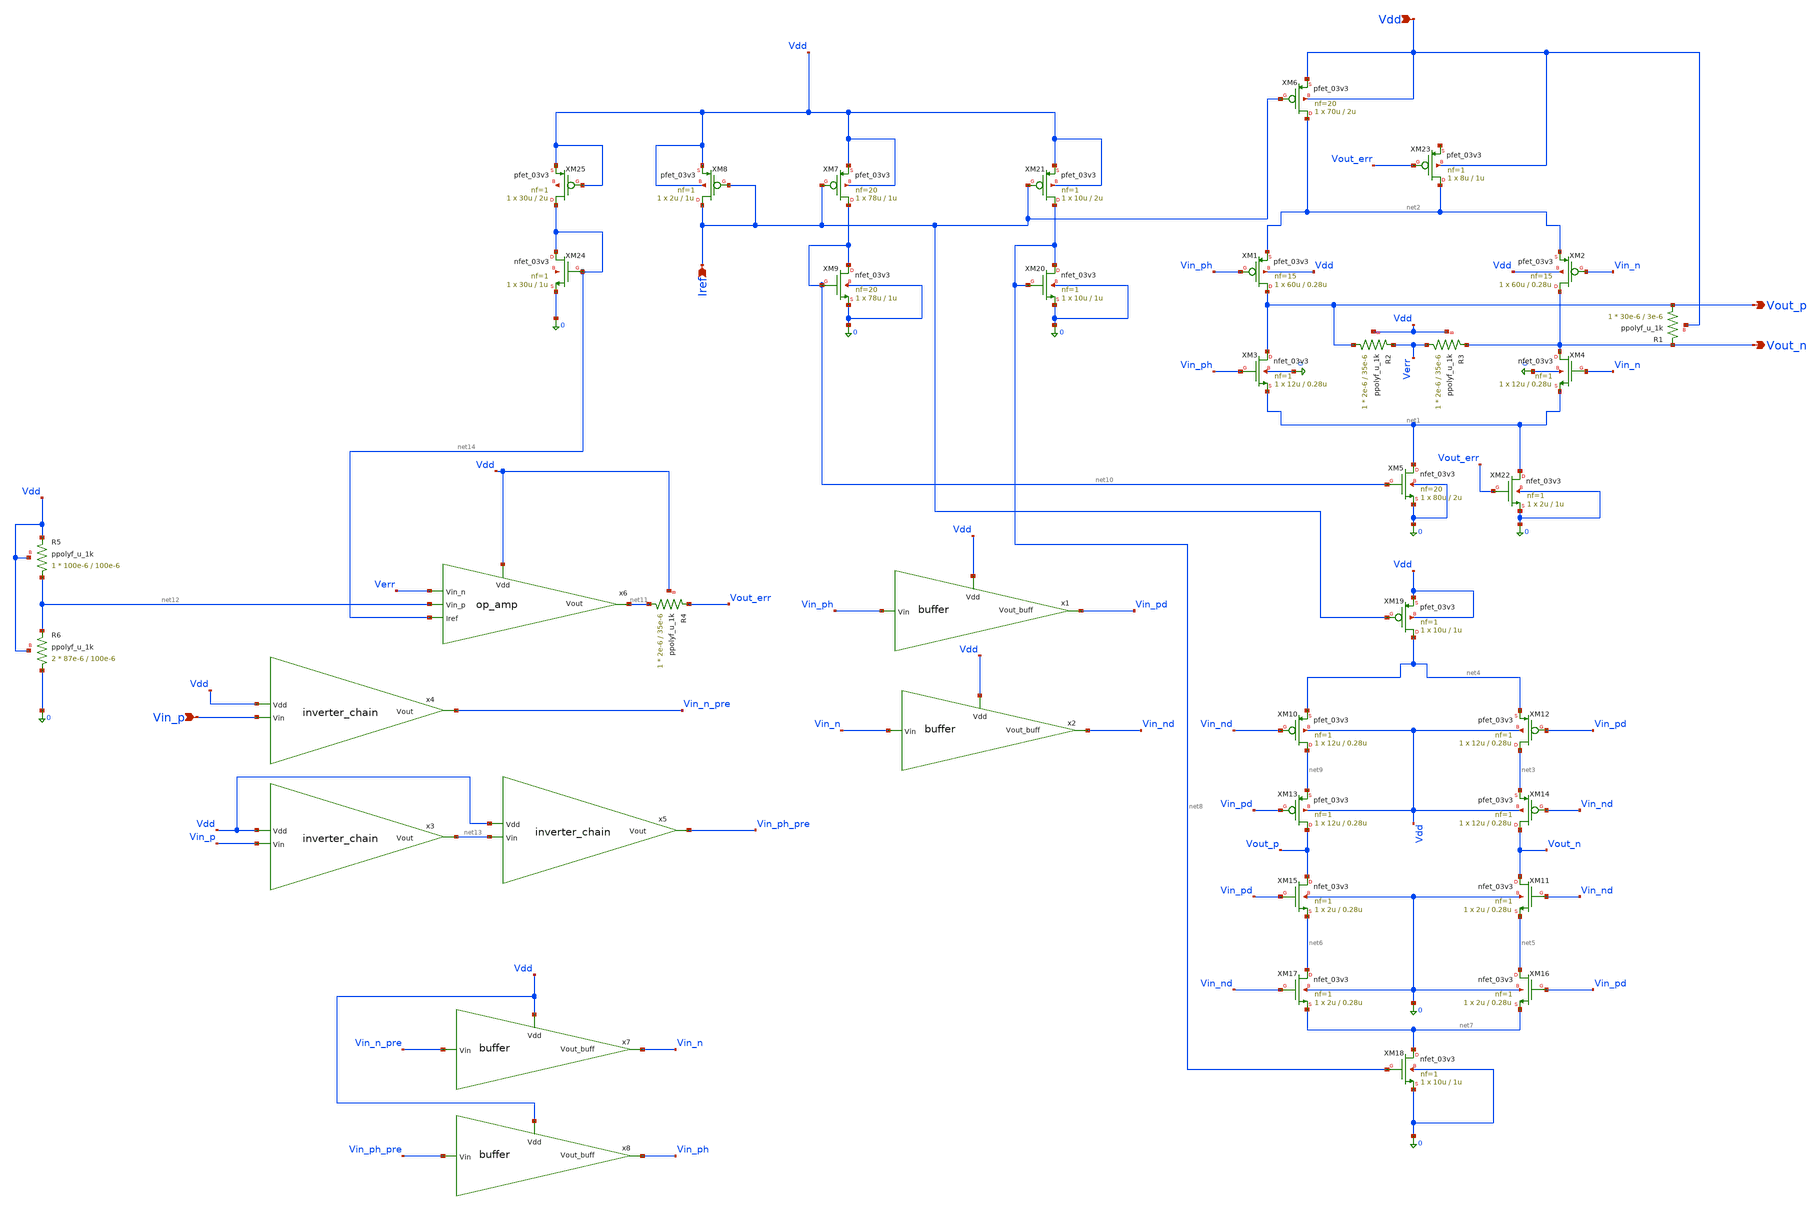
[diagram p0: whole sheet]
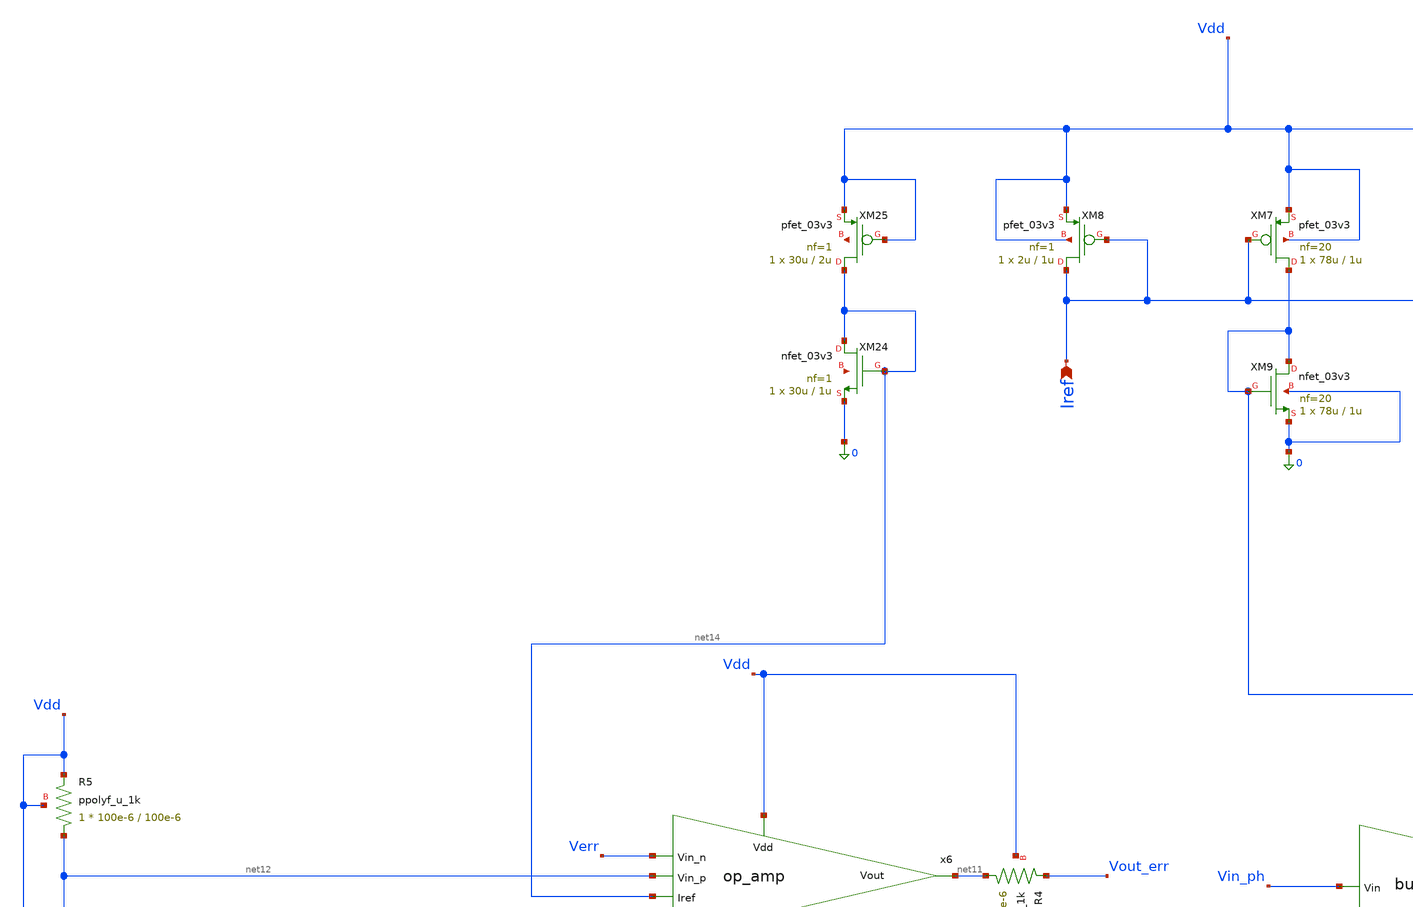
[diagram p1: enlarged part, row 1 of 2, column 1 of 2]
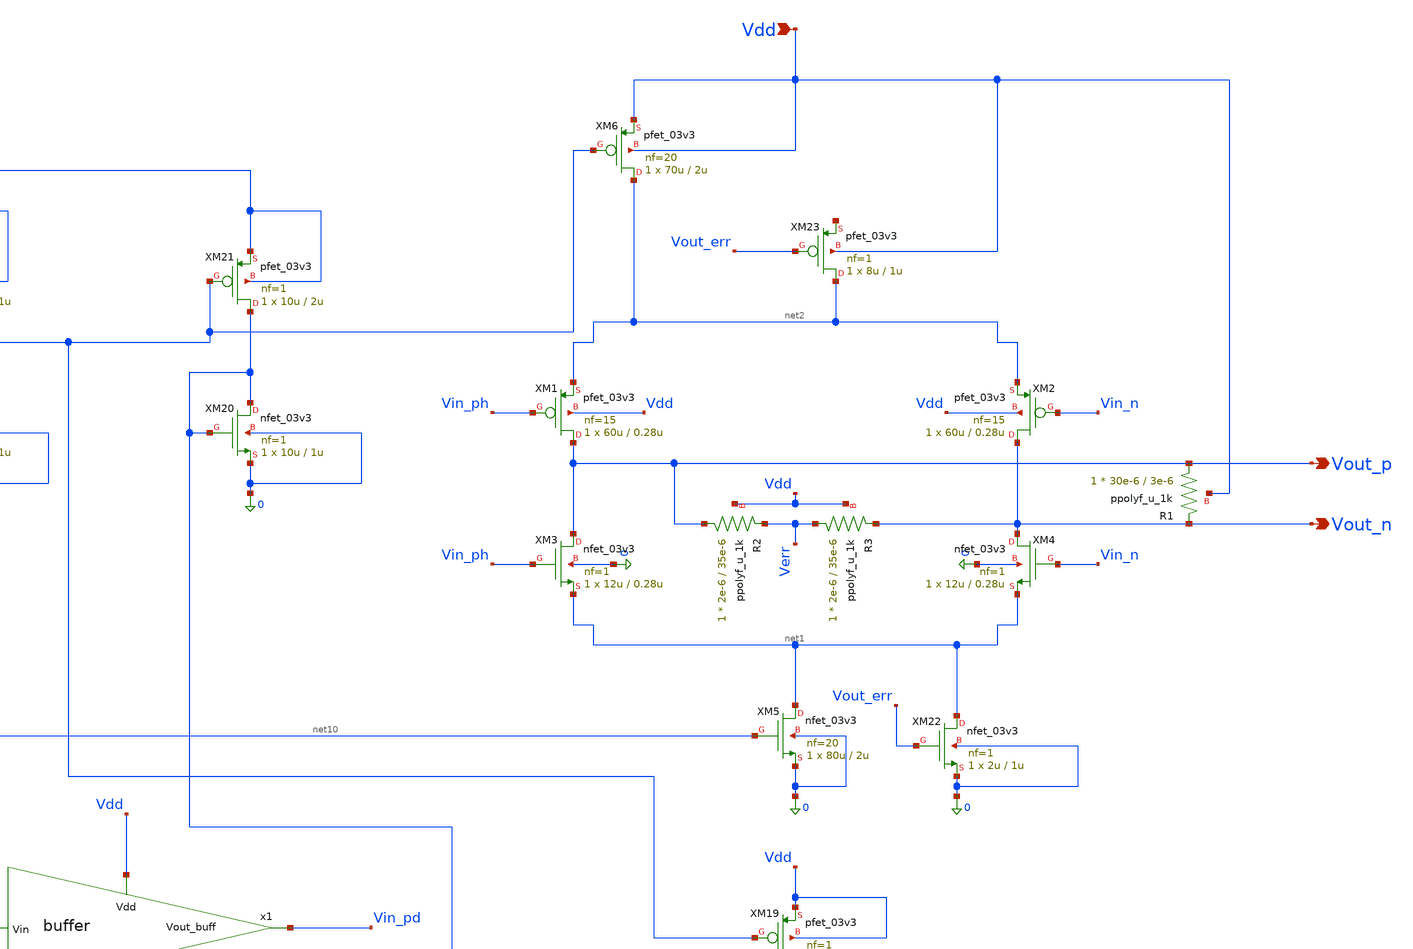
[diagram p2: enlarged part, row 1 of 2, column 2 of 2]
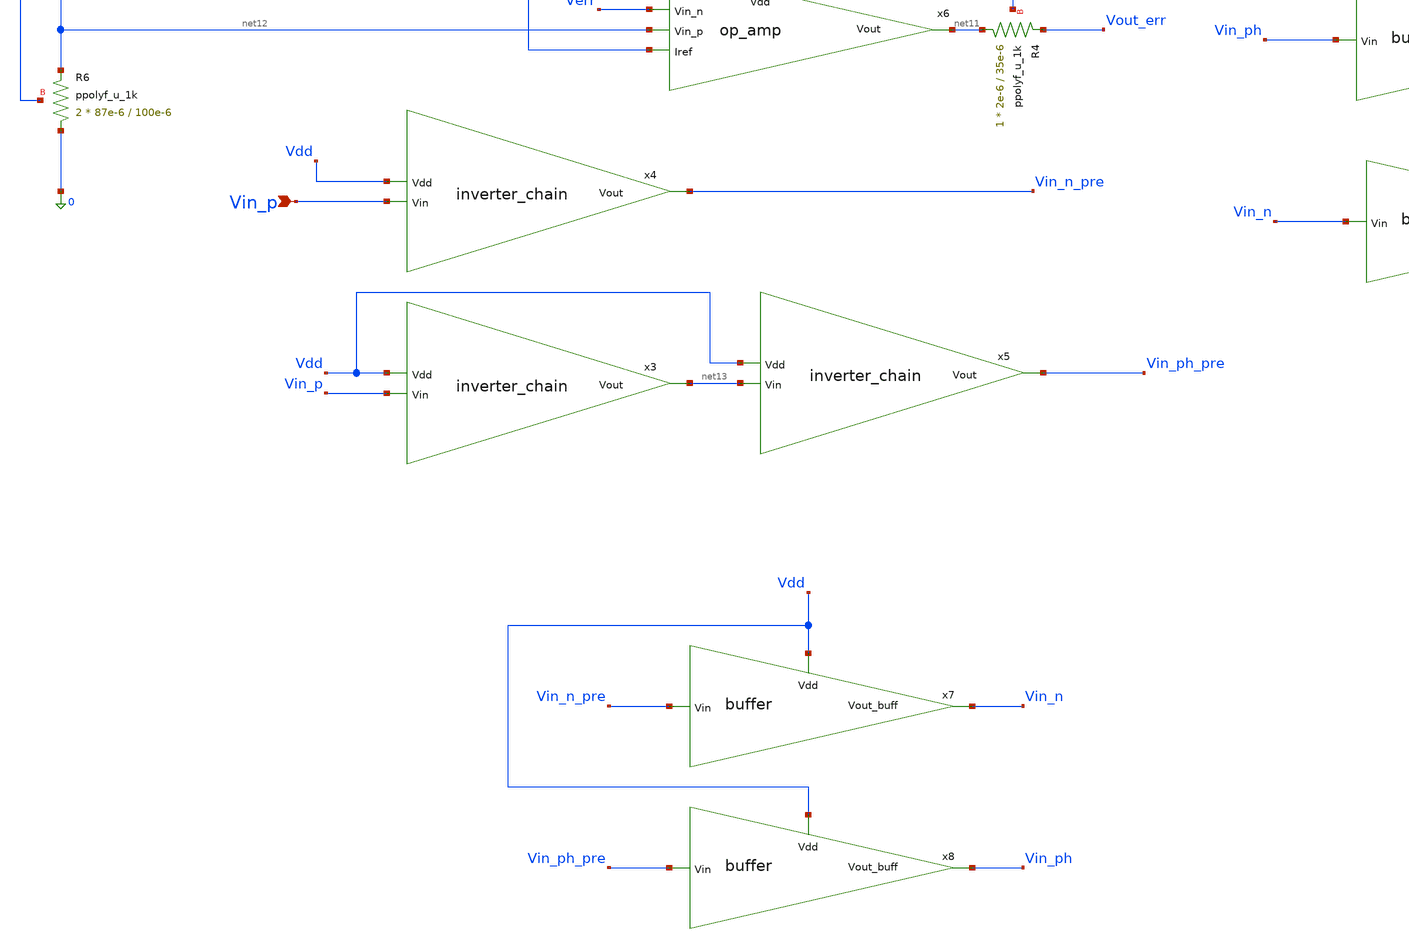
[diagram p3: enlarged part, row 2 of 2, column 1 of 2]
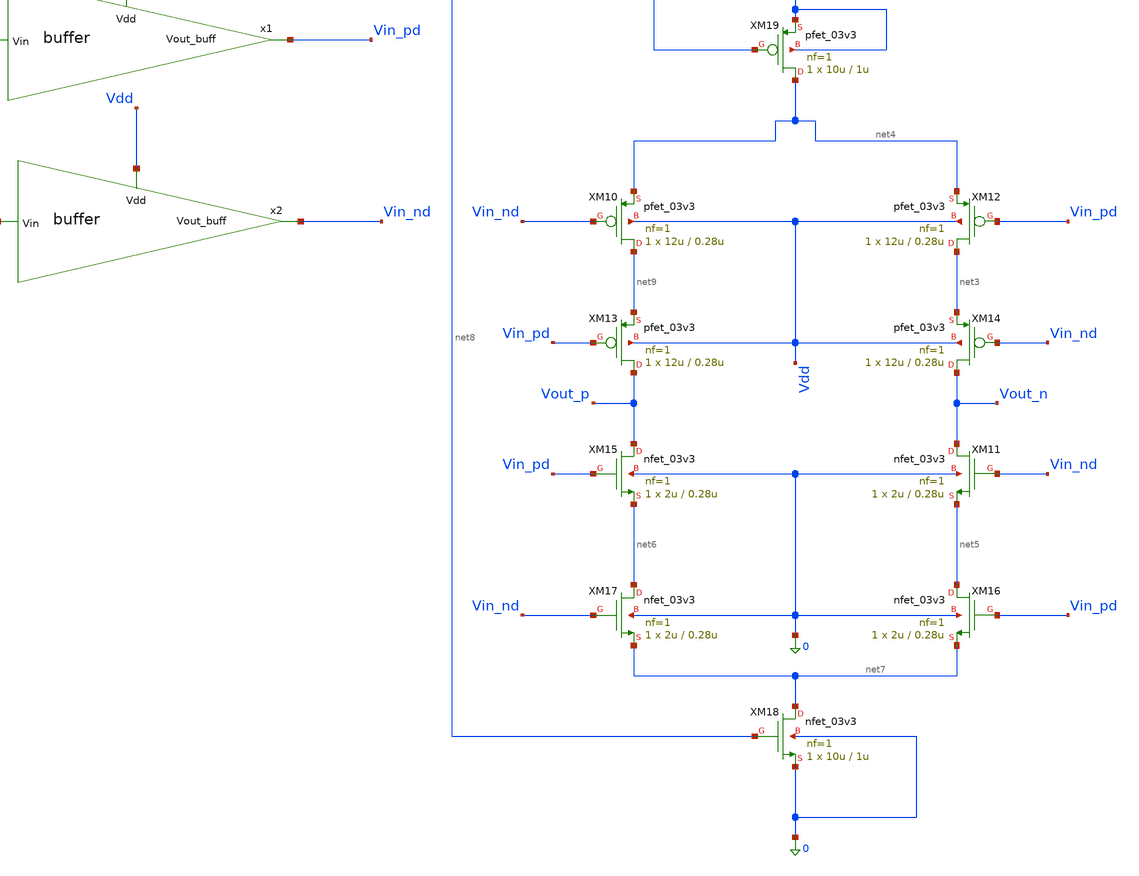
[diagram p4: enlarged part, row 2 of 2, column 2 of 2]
** sch_path: blocks/adc/lvds/lvds_v5.sch
**.subckt lvds_v5 Vdd Iref Vin_p Vout_n Vout_p
*.ipin Vdd
*.ipin Iref
*.ipin Vin_p
*.opin Vout_n
*.opin Vout_p
XM1 Vout_p Vin_ph net2 Vdd pfet_03v3 L=0.28u W=60u nf=15 ad='int((nf+1)/2) * W/nf * 0.18u' as='int((nf+2)/2) * W/nf * 0.18u'
+ pd='2*int((nf+1)/2) * (W/nf + 0.18u)' ps='2*int((nf+2)/2) * (W/nf + 0.18u)' nrd='0.18u / W' nrs='0.18u / W'
+ sa=0 sb=0 sd=0 m=1
XM2 Vout_n Vin_n net2 Vdd pfet_03v3 L=0.28u W=60u nf=15 ad='int((nf+1)/2) * W/nf * 0.18u' as='int((nf+2)/2) * W/nf * 0.18u'
+ pd='2*int((nf+1)/2) * (W/nf + 0.18u)' ps='2*int((nf+2)/2) * (W/nf + 0.18u)' nrd='0.18u / W' nrs='0.18u / W'
+ sa=0 sb=0 sd=0 m=1
XM3 Vout_p Vin_ph net1 0 nfet_03v3 L=0.28u W=12u nf=1 ad='int((nf+1)/2) * W/nf * 0.18u' as='int((nf+2)/2) * W/nf * 0.18u'
+ pd='2*int((nf+1)/2) * (W/nf + 0.18u)' ps='2*int((nf+2)/2) * (W/nf + 0.18u)' nrd='0.18u / W' nrs='0.18u / W'
+ sa=0 sb=0 sd=0 m=1
XM4 Vout_n Vin_n net1 0 nfet_03v3 L=0.28u W=12u nf=1 ad='int((nf+1)/2) * W/nf * 0.18u' as='int((nf+2)/2) * W/nf * 0.18u'
+ pd='2*int((nf+1)/2) * (W/nf + 0.18u)' ps='2*int((nf+2)/2) * (W/nf + 0.18u)' nrd='0.18u / W' nrs='0.18u / W'
+ sa=0 sb=0 sd=0 m=1
XM5 net1 net10 0 0 nfet_03v3 L=2u W=80u nf=20 ad='int((nf+1)/2) * W/nf * 0.18u' as='int((nf+2)/2) * W/nf * 0.18u'
+ pd='2*int((nf+1)/2) * (W/nf + 0.18u)' ps='2*int((nf+2)/2) * (W/nf + 0.18u)' nrd='0.18u / W' nrs='0.18u / W'
+ sa=0 sb=0 sd=0 m=1
XM6 net2 Iref Vdd Vdd pfet_03v3 L=2u W=70u nf=20 ad='int((nf+1)/2) * W/nf * 0.18u' as='int((nf+2)/2) * W/nf * 0.18u'
+ pd='2*int((nf+1)/2) * (W/nf + 0.18u)' ps='2*int((nf+2)/2) * (W/nf + 0.18u)' nrd='0.18u / W' nrs='0.18u / W'
+ sa=0 sb=0 sd=0 m=1
XM8 Iref Iref Vdd Vdd pfet_03v3 L=1u W=2u nf=1 ad='int((nf+1)/2) * W/nf * 0.18u' as='int((nf+2)/2) * W/nf * 0.18u'
+ pd='2*int((nf+1)/2) * (W/nf + 0.18u)' ps='2*int((nf+2)/2) * (W/nf + 0.18u)' nrd='0.18u / W' nrs='0.18u / W'
+ sa=0 sb=0 sd=0 m=1
XM10 net9 Vin_nd net4 Vdd pfet_03v3 L=0.28u W=12u nf=1 ad='int((nf+1)/2) * W/nf * 0.18u' as='int((nf+2)/2) * W/nf * 0.18u'
+ pd='2*int((nf+1)/2) * (W/nf + 0.18u)' ps='2*int((nf+2)/2) * (W/nf + 0.18u)' nrd='0.18u / W' nrs='0.18u / W'
+ sa=0 sb=0 sd=0 m=1
XM11 Vout_n Vin_nd net5 0 nfet_03v3 L=0.28u W=2u nf=1 ad='int((nf+1)/2) * W/nf * 0.18u' as='int((nf+2)/2) * W/nf * 0.18u'
+ pd='2*int((nf+1)/2) * (W/nf + 0.18u)' ps='2*int((nf+2)/2) * (W/nf + 0.18u)' nrd='0.18u / W' nrs='0.18u / W'
+ sa=0 sb=0 sd=0 m=1
XM12 net3 Vin_pd net4 Vdd pfet_03v3 L=0.28u W=12u nf=1 ad='int((nf+1)/2) * W/nf * 0.18u' as='int((nf+2)/2) * W/nf * 0.18u'
+ pd='2*int((nf+1)/2) * (W/nf + 0.18u)' ps='2*int((nf+2)/2) * (W/nf + 0.18u)' nrd='0.18u / W' nrs='0.18u / W'
+ sa=0 sb=0 sd=0 m=1
XM13 Vout_p Vin_pd net9 Vdd pfet_03v3 L=0.28u W=12u nf=1 ad='int((nf+1)/2) * W/nf * 0.18u' as='int((nf+2)/2) * W/nf * 0.18u'
+ pd='2*int((nf+1)/2) * (W/nf + 0.18u)' ps='2*int((nf+2)/2) * (W/nf + 0.18u)' nrd='0.18u / W' nrs='0.18u / W'
+ sa=0 sb=0 sd=0 m=1
XM14 Vout_n Vin_nd net3 Vdd pfet_03v3 L=0.28u W=12u nf=1 ad='int((nf+1)/2) * W/nf * 0.18u' as='int((nf+2)/2) * W/nf * 0.18u'
+ pd='2*int((nf+1)/2) * (W/nf + 0.18u)' ps='2*int((nf+2)/2) * (W/nf + 0.18u)' nrd='0.18u / W' nrs='0.18u / W'
+ sa=0 sb=0 sd=0 m=1
XM15 Vout_p Vin_pd net6 0 nfet_03v3 L=0.28u W=2u nf=1 ad='int((nf+1)/2) * W/nf * 0.18u' as='int((nf+2)/2) * W/nf * 0.18u'
+ pd='2*int((nf+1)/2) * (W/nf + 0.18u)' ps='2*int((nf+2)/2) * (W/nf + 0.18u)' nrd='0.18u / W' nrs='0.18u / W'
+ sa=0 sb=0 sd=0 m=1
XM16 net5 Vin_pd net7 0 nfet_03v3 L=0.28u W=2u nf=1 ad='int((nf+1)/2) * W/nf * 0.18u' as='int((nf+2)/2) * W/nf * 0.18u'
+ pd='2*int((nf+1)/2) * (W/nf + 0.18u)' ps='2*int((nf+2)/2) * (W/nf + 0.18u)' nrd='0.18u / W' nrs='0.18u / W'
+ sa=0 sb=0 sd=0 m=1
XM17 net6 Vin_nd net7 0 nfet_03v3 L=0.28u W=2u nf=1 ad='int((nf+1)/2) * W/nf * 0.18u' as='int((nf+2)/2) * W/nf * 0.18u'
+ pd='2*int((nf+1)/2) * (W/nf + 0.18u)' ps='2*int((nf+2)/2) * (W/nf + 0.18u)' nrd='0.18u / W' nrs='0.18u / W'
+ sa=0 sb=0 sd=0 m=1
XM18 net7 net8 0 0 nfet_03v3 L=1u W=10u nf=1 ad='int((nf+1)/2) * W/nf * 0.18u' as='int((nf+2)/2) * W/nf * 0.18u'
+ pd='2*int((nf+1)/2) * (W/nf + 0.18u)' ps='2*int((nf+2)/2) * (W/nf + 0.18u)' nrd='0.18u / W' nrs='0.18u / W'
+ sa=0 sb=0 sd=0 m=1
XM19 net4 Iref Vdd Vdd pfet_03v3 L=1u W=10u nf=1 ad='int((nf+1)/2) * W/nf * 0.18u' as='int((nf+2)/2) * W/nf * 0.18u'
+ pd='2*int((nf+1)/2) * (W/nf + 0.18u)' ps='2*int((nf+2)/2) * (W/nf + 0.18u)' nrd='0.18u / W' nrs='0.18u / W'
+ sa=0 sb=0 sd=0 m=1
XM21 net8 Iref Vdd Vdd pfet_03v3 L=2u W=10u nf=1 ad='int((nf+1)/2) * W/nf * 0.18u' as='int((nf+2)/2) * W/nf * 0.18u'
+ pd='2*int((nf+1)/2) * (W/nf + 0.18u)' ps='2*int((nf+2)/2) * (W/nf + 0.18u)' nrd='0.18u / W' nrs='0.18u / W'
+ sa=0 sb=0 sd=0 m=1
XM20 net8 net8 0 0 nfet_03v3 L=1u W=10u nf=1 ad='int((nf+1)/2) * W/nf * 0.18u' as='int((nf+2)/2) * W/nf * 0.18u'
+ pd='2*int((nf+1)/2) * (W/nf + 0.18u)' ps='2*int((nf+2)/2) * (W/nf + 0.18u)' nrd='0.18u / W' nrs='0.18u / W'
+ sa=0 sb=0 sd=0 m=1
XR2 Vout_p Verr Vdd ppolyf_u_1k r_width=2e-6 r_length=35e-6 m=1
XR3 Verr Vout_n Vdd ppolyf_u_1k r_width=2e-6 r_length=35e-6 m=1
XM7 net10 Iref Vdd Vdd pfet_03v3 L=1u W=78u nf=20 ad='int((nf+1)/2) * W/nf * 0.18u' as='int((nf+2)/2) * W/nf * 0.18u'
+ pd='2*int((nf+1)/2) * (W/nf + 0.18u)' ps='2*int((nf+2)/2) * (W/nf + 0.18u)' nrd='0.18u / W' nrs='0.18u / W'
+ sa=0 sb=0 sd=0 m=1
XM9 net10 net10 0 0 nfet_03v3 L=1u W=78u nf=20 ad='int((nf+1)/2) * W/nf * 0.18u' as='int((nf+2)/2) * W/nf * 0.18u'
+ pd='2*int((nf+1)/2) * (W/nf + 0.18u)' ps='2*int((nf+2)/2) * (W/nf + 0.18u)' nrd='0.18u / W' nrs='0.18u / W'
+ sa=0 sb=0 sd=0 m=1
x4 Vdd Vin_n_pre Vin_p inverter_chain
XM22 net1 Vout_err 0 0 nfet_03v3 L=1u W=2u nf=1 ad='int((nf+1)/2) * W/nf * 0.18u' as='int((nf+2)/2) * W/nf * 0.18u'
+ pd='2*int((nf+1)/2) * (W/nf + 0.18u)' ps='2*int((nf+2)/2) * (W/nf + 0.18u)' nrd='0.18u / W' nrs='0.18u / W'
+ sa=0 sb=0 sd=0 m=1
XM23 net2 Vout_err net15 Vdd pfet_03v3 L=1u W=8u nf=1 ad='int((nf+1)/2) * W/nf * 0.18u' as='int((nf+2)/2) * W/nf * 0.18u'
+ pd='2*int((nf+1)/2) * (W/nf + 0.18u)' ps='2*int((nf+2)/2) * (W/nf + 0.18u)' nrd='0.18u / W' nrs='0.18u / W'
+ sa=0 sb=0 sd=0 m=1
x3 Vdd net13 Vin_p inverter_chain
x5 Vdd Vin_ph_pre net13 inverter_chain
x7 Vdd Vin_n Vin_n_pre buffer
x8 Vdd Vin_ph Vin_ph_pre buffer
XM24 net14 net14 0 net16 nfet_03v3 L=1u W=30u nf=1 ad='int((nf+1)/2) * W/nf * 0.18u' as='int((nf+2)/2) * W/nf * 0.18u'
+ pd='2*int((nf+1)/2) * (W/nf + 0.18u)' ps='2*int((nf+2)/2) * (W/nf + 0.18u)' nrd='0.18u / W' nrs='0.18u / W'
+ sa=0 sb=0 sd=0 m=1
XM25 net14 Vdd Vdd net17 pfet_03v3 L=2u W=30u nf=1 ad='int((nf+1)/2) * W/nf * 0.18u' as='int((nf+2)/2) * W/nf * 0.18u'
+ pd='2*int((nf+1)/2) * (W/nf + 0.18u)' ps='2*int((nf+2)/2) * (W/nf + 0.18u)' nrd='0.18u / W' nrs='0.18u / W'
+ sa=0 sb=0 sd=0 m=1
x1 Vdd Vin_pd Vin_ph buffer
x2 Vdd Vin_nd Vin_n buffer
XR4 net11 Vout_err Vdd ppolyf_u_1k r_width=2e-6 r_length=35e-6 m=1
x6 Vdd net11 Verr net12 net14 op_amp
XR1 Vout_p Vout_n Vdd ppolyf_u_1k r_width=30e-6 r_length=3e-6 m=1
XR5 net12 Vdd Vdd ppolyf_u_1k r_width=100e-6 r_length=100e-6 m=1
XR6 0 net12 Vdd ppolyf_u_1k r_width=87e-6 r_length=100e-6 m=2
**.ends
.end
